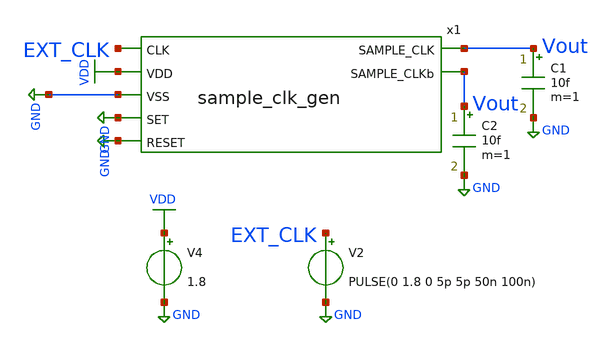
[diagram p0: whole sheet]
** sch_path: module/jh_temp_dir/sample_clk_gen/tb_sample_clk_gen.sch
**.subckt tb_sample_clk_gen
V2 EXT_CLK GND PULSE(0 1.8 0 5p 5p 50n 100n)
V4 VDD GND 1.8
x1 Vout Vout EXT_CLK VDD GND GND GND sample_clk_gen
C1 Vout GND 10f m=1
C2 Vout GND 10f m=1
**** begin user architecture code



.lib /foss/pdks/sky130A/libs.tech/ngspice/sky130.lib.spice tt

.tran 1ps 400ns

.control
	run
	plot V(Vout) V(EXT_CLK)
.endc
.save all



**** end user architecture code
**.ends
.GLOBAL GND
.GLOBAL VDD
.end
